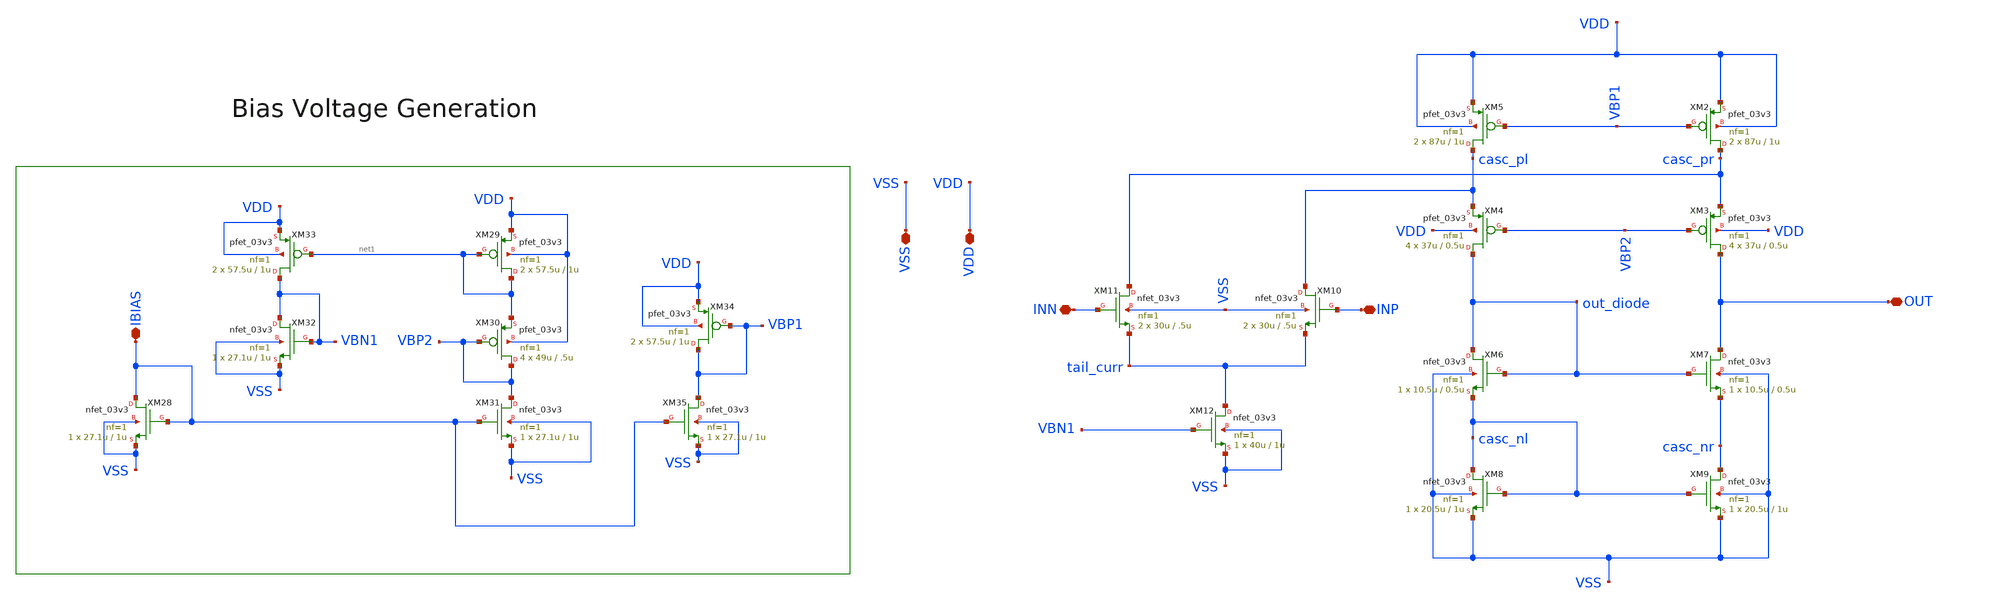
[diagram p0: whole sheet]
** sch_path: designs/etj_folded_new_sym.sch
**.subckt etj_folded_new_sym OUT IBIAS VSS VDD INN INP
*.iopin OUT
*.iopin IBIAS
*.iopin VSS
*.iopin VDD
*.iopin INN
*.iopin INP
XM2 casc_pr VBP1 VDD VDD pfet_03v3 L=1u W=87u nf=1 ad='int((nf+1)/2) * W/nf * 0.18u' as='int((nf+2)/2) * W/nf * 0.18u'
+ pd='2*int((nf+1)/2) * (W/nf + 0.18u)' ps='2*int((nf+2)/2) * (W/nf + 0.18u)' nrd='0.18u / W' nrs='0.18u / W'
+ sa=0 sb=0 sd=0 m=2
XM3 OUT VBP2 casc_pr VDD pfet_03v3 L=0.5u W=37u nf=1 ad='int((nf+1)/2) * W/nf * 0.18u' as='int((nf+2)/2) * W/nf * 0.18u'
+ pd='2*int((nf+1)/2) * (W/nf + 0.18u)' ps='2*int((nf+2)/2) * (W/nf + 0.18u)' nrd='0.18u / W' nrs='0.18u / W'
+ sa=0 sb=0 sd=0 m=4
XM4 out_diode VBP2 casc_pl VDD pfet_03v3 L=0.5u W=37u nf=1 ad='int((nf+1)/2) * W/nf * 0.18u' as='int((nf+2)/2) * W/nf * 0.18u'
+ pd='2*int((nf+1)/2) * (W/nf + 0.18u)' ps='2*int((nf+2)/2) * (W/nf + 0.18u)' nrd='0.18u / W' nrs='0.18u / W'
+ sa=0 sb=0 sd=0 m=4
XM5 casc_pl VBP1 VDD VDD pfet_03v3 L=1u W=87u nf=1 ad='int((nf+1)/2) * W/nf * 0.18u' as='int((nf+2)/2) * W/nf * 0.18u'
+ pd='2*int((nf+1)/2) * (W/nf + 0.18u)' ps='2*int((nf+2)/2) * (W/nf + 0.18u)' nrd='0.18u / W' nrs='0.18u / W'
+ sa=0 sb=0 sd=0 m=2
XM6 out_diode out_diode casc_nl VSS nfet_03v3 L=0.5u W=10.5u nf=1 ad='int((nf+1)/2) * W/nf * 0.18u' as='int((nf+2)/2) * W/nf * 0.18u'
+ pd='2*int((nf+1)/2) * (W/nf + 0.18u)' ps='2*int((nf+2)/2) * (W/nf + 0.18u)' nrd='0.18u / W' nrs='0.18u / W'
+ sa=0 sb=0 sd=0 m=1
XM7 OUT out_diode casc_nr VSS nfet_03v3 L=0.5u W=10.5u nf=1 ad='int((nf+1)/2) * W/nf * 0.18u' as='int((nf+2)/2) * W/nf * 0.18u'
+ pd='2*int((nf+1)/2) * (W/nf + 0.18u)' ps='2*int((nf+2)/2) * (W/nf + 0.18u)' nrd='0.18u / W' nrs='0.18u / W'
+ sa=0 sb=0 sd=0 m=1
XM8 casc_nl casc_nl VSS VSS nfet_03v3 L=1u W=20.5u nf=1 ad='int((nf+1)/2) * W/nf * 0.18u' as='int((nf+2)/2) * W/nf * 0.18u'
+ pd='2*int((nf+1)/2) * (W/nf + 0.18u)' ps='2*int((nf+2)/2) * (W/nf + 0.18u)' nrd='0.18u / W' nrs='0.18u / W'
+ sa=0 sb=0 sd=0 m=1
XM9 casc_nr casc_nl VSS VSS nfet_03v3 L=1u W=20.5u nf=1 ad='int((nf+1)/2) * W/nf * 0.18u' as='int((nf+2)/2) * W/nf * 0.18u'
+ pd='2*int((nf+1)/2) * (W/nf + 0.18u)' ps='2*int((nf+2)/2) * (W/nf + 0.18u)' nrd='0.18u / W' nrs='0.18u / W'
+ sa=0 sb=0 sd=0 m=1
XM10 casc_pl INP tail_curr VSS nfet_03v3 L=.5u W=30u nf=1 ad='int((nf+1)/2) * W/nf * 0.18u' as='int((nf+2)/2) * W/nf * 0.18u'
+ pd='2*int((nf+1)/2) * (W/nf + 0.18u)' ps='2*int((nf+2)/2) * (W/nf + 0.18u)' nrd='0.18u / W' nrs='0.18u / W'
+ sa=0 sb=0 sd=0 m=2
XM12 tail_curr VBN1 VSS VSS nfet_03v3 L=1u W=40u nf=1 ad='int((nf+1)/2) * W/nf * 0.18u' as='int((nf+2)/2) * W/nf * 0.18u'
+ pd='2*int((nf+1)/2) * (W/nf + 0.18u)' ps='2*int((nf+2)/2) * (W/nf + 0.18u)' nrd='0.18u / W' nrs='0.18u / W'
+ sa=0 sb=0 sd=0 m=1
XM11 casc_pr INN tail_curr VSS nfet_03v3 L=.5u W=30u nf=1 ad='int((nf+1)/2) * W/nf * 0.18u' as='int((nf+2)/2) * W/nf * 0.18u'
+ pd='2*int((nf+1)/2) * (W/nf + 0.18u)' ps='2*int((nf+2)/2) * (W/nf + 0.18u)' nrd='0.18u / W' nrs='0.18u / W'
+ sa=0 sb=0 sd=0 m=2
XM28 IBIAS IBIAS VSS VSS nfet_03v3 L=1u W=27.1u nf=1 ad='int((nf+1)/2) * W/nf * 0.18u' as='int((nf+2)/2) * W/nf * 0.18u'
+ pd='2*int((nf+1)/2) * (W/nf + 0.18u)' ps='2*int((nf+2)/2) * (W/nf + 0.18u)' nrd='0.18u / W' nrs='0.18u / W'
+ sa=0 sb=0 sd=0 m=1
XM29 net1 net1 VDD VDD pfet_03v3 L=1u W=57.5u nf=1 ad='int((nf+1)/2) * W/nf * 0.18u' as='int((nf+2)/2) * W/nf * 0.18u'
+ pd='2*int((nf+1)/2) * (W/nf + 0.18u)' ps='2*int((nf+2)/2) * (W/nf + 0.18u)' nrd='0.18u / W' nrs='0.18u / W'
+ sa=0 sb=0 sd=0 m=2
XM30 VBP2 VBP2 net1 VDD pfet_03v3 L=.5u W=49u nf=1 ad='int((nf+1)/2) * W/nf * 0.18u' as='int((nf+2)/2) * W/nf * 0.18u'
+ pd='2*int((nf+1)/2) * (W/nf + 0.18u)' ps='2*int((nf+2)/2) * (W/nf + 0.18u)' nrd='0.18u / W' nrs='0.18u / W'
+ sa=0 sb=0 sd=0 m=4
XM31 VBP2 IBIAS VSS VSS nfet_03v3 L=1u W=27.1u nf=1 ad='int((nf+1)/2) * W/nf * 0.18u' as='int((nf+2)/2) * W/nf * 0.18u'
+ pd='2*int((nf+1)/2) * (W/nf + 0.18u)' ps='2*int((nf+2)/2) * (W/nf + 0.18u)' nrd='0.18u / W' nrs='0.18u / W'
+ sa=0 sb=0 sd=0 m=1
XM32 VBN1 VBN1 VSS VSS nfet_03v3 L=1u W=27.1u nf=1 ad='int((nf+1)/2) * W/nf * 0.18u' as='int((nf+2)/2) * W/nf * 0.18u'
+ pd='2*int((nf+1)/2) * (W/nf + 0.18u)' ps='2*int((nf+2)/2) * (W/nf + 0.18u)' nrd='0.18u / W' nrs='0.18u / W'
+ sa=0 sb=0 sd=0 m=1
XM33 VBN1 net1 VDD VDD pfet_03v3 L=1u W=57.5u nf=1 ad='int((nf+1)/2) * W/nf * 0.18u' as='int((nf+2)/2) * W/nf * 0.18u'
+ pd='2*int((nf+1)/2) * (W/nf + 0.18u)' ps='2*int((nf+2)/2) * (W/nf + 0.18u)' nrd='0.18u / W' nrs='0.18u / W'
+ sa=0 sb=0 sd=0 m=2
XM34 VBP1 VBP1 VDD VDD pfet_03v3 L=1u W=57.5u nf=1 ad='int((nf+1)/2) * W/nf * 0.18u' as='int((nf+2)/2) * W/nf * 0.18u'
+ pd='2*int((nf+1)/2) * (W/nf + 0.18u)' ps='2*int((nf+2)/2) * (W/nf + 0.18u)' nrd='0.18u / W' nrs='0.18u / W'
+ sa=0 sb=0 sd=0 m=2
XM35 VBP1 IBIAS VSS VSS nfet_03v3 L=1u W=27.1u nf=1 ad='int((nf+1)/2) * W/nf * 0.18u' as='int((nf+2)/2) * W/nf * 0.18u'
+ pd='2*int((nf+1)/2) * (W/nf + 0.18u)' ps='2*int((nf+2)/2) * (W/nf + 0.18u)' nrd='0.18u / W' nrs='0.18u / W'
+ sa=0 sb=0 sd=0 m=1
**.ends
.end
